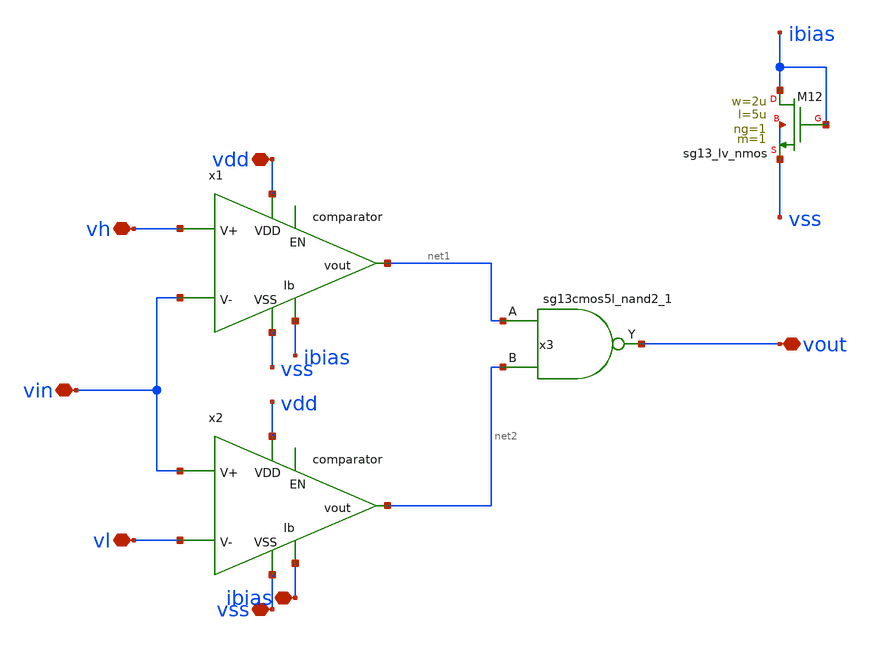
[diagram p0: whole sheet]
** sch_path: schematic/xschem/wind_comp/wind_comp.sch
**.subckt wind_comp vdd vout vl vh ibias vss vin
*.iopin vdd
*.iopin vout
*.iopin vl
*.iopin vh
*.iopin ibias
*.iopin vss
*.iopin vin
x1 vdd net1 vh vin ibias vss comparator
x2 vdd net2 vin vl ibias vss comparator
x3 vout net1 net2 VDD VSS sg13g2_nand2_1
XM12 ibias ibias vss vss sg13_lv_nmos w=2u l=5u ng=1 m=1 mm_ok=1
**.ends

* expanding   symbol:  comparator/comparator.sym # of pins=6
** sym_path: schematic/xschem/comparator/comparator.sym
** sch_path: schematic/xschem/comparator/comparator.sch
.subckt comparator vdd vout v- v+ iout vss
*.iopin vdd
*.iopin vss
*.iopin v-
*.iopin v+
*.iopin iout
*.iopin vout
XM6 votap v+ net1 vss sg13_lv_nmos w=0.26u l=3u ng=1 m=2 mm_ok=1
XM8 vdd votap votap vdd sg13_lv_pmos w=0.35u l=1u ng=1 m=2 mm_ok=1
XM9 votan v- net1 vss sg13_lv_nmos w=0.26u l=3u ng=1 m=2 mm_ok=1
XM10 vdd votan votan vdd sg13_lv_pmos w=0.35u l=1u ng=1 m=2 mm_ok=1
XM11 net1 iout vss vss sg13_lv_nmos w=2u l=5u ng=1 m=2 mm_ok=1
x1 vdd votan vom vop vss vss decision_circuit
x2 vdd votap vop vom vss vss decision_circuit
x3 net3 net2 VDD VSS sg13g2_inv_16
x4 vdd iout vop vom net2 vss final_stage_ota
x5 vout net3 VDD VSS sg13g2_inv_16
.ends


* expanding   symbol:  decision_circuit/decision_circuit.sym # of pins=6
** sym_path: schematic/xschem/decision_circuit/decision_circuit.sym
** sch_path: schematic/xschem/decision_circuit/decision_circuit.sch
.subckt decision_circuit vdd vota vout vota_n vss shift
*.iopin vota
*.iopin shift
*.iopin vota_n
*.iopin vdd
*.iopin vss
*.iopin vout
XM1 vout vota vdd vdd sg13_lv_pmos w=0.7u l=1u ng=1 m=1 mm_ok=1
XM2 vout vout shift vss sg13_lv_nmos w=0.26u l=10u ng=1 m=2 mm_ok=1
XM3 vout vota_n shift vss sg13_lv_nmos w=0.26u l=10u ng=1 m=2 mm_ok=1
XM4 vss vss vout vss sg13_lv_nmos w=0.26u l=0.5u ng=1 m=4 mm_ok=1
XM5 vdd vdd vout vdd sg13_lv_pmos w=0.35u l=0.5u ng=1 m=2 mm_ok=1
.ends


* expanding   symbol:  final_stage_ota/final_stage_ota.sym # of pins=6
** sym_path: schematic/xschem/final_stage_ota/final_stage_ota.sym
** sch_path: schematic/xschem/final_stage_ota/final_stage_ota.sch
.subckt final_stage_ota vdd iout vop vom vout vss
*.iopin vdd
*.iopin vom
*.iopin vop
*.iopin vss
*.iopin vout
*.iopin iout
XM1 vdd ibp vt vdd sg13_lv_pmos w=1u l=3u ng=1 m=2 mm_ok=1
XM2 net1 net1 vss vss sg13_lv_nmos w=0.15u l=3u ng=1 m=2 mm_ok=1
XM3 vt vom net1 vdd sg13_lv_pmos w=3.12u l=1u ng=1 m=2 mm_ok=1
XM4 vout net1 vss vss sg13_lv_nmos w=0.15u l=3u ng=1 m=2 mm_ok=1
XM5 vt vop vout vdd sg13_lv_pmos w=3.12u l=1u ng=1 m=2 mm_ok=1
XM6 ibp iout vss vss sg13_lv_nmos w=2u l=5u ng=1 m=1 mm_ok=1
XM7 vdd ibp ibp vdd sg13_lv_pmos w=1u l=3u ng=1 m=1 mm_ok=1
.ends

.end
